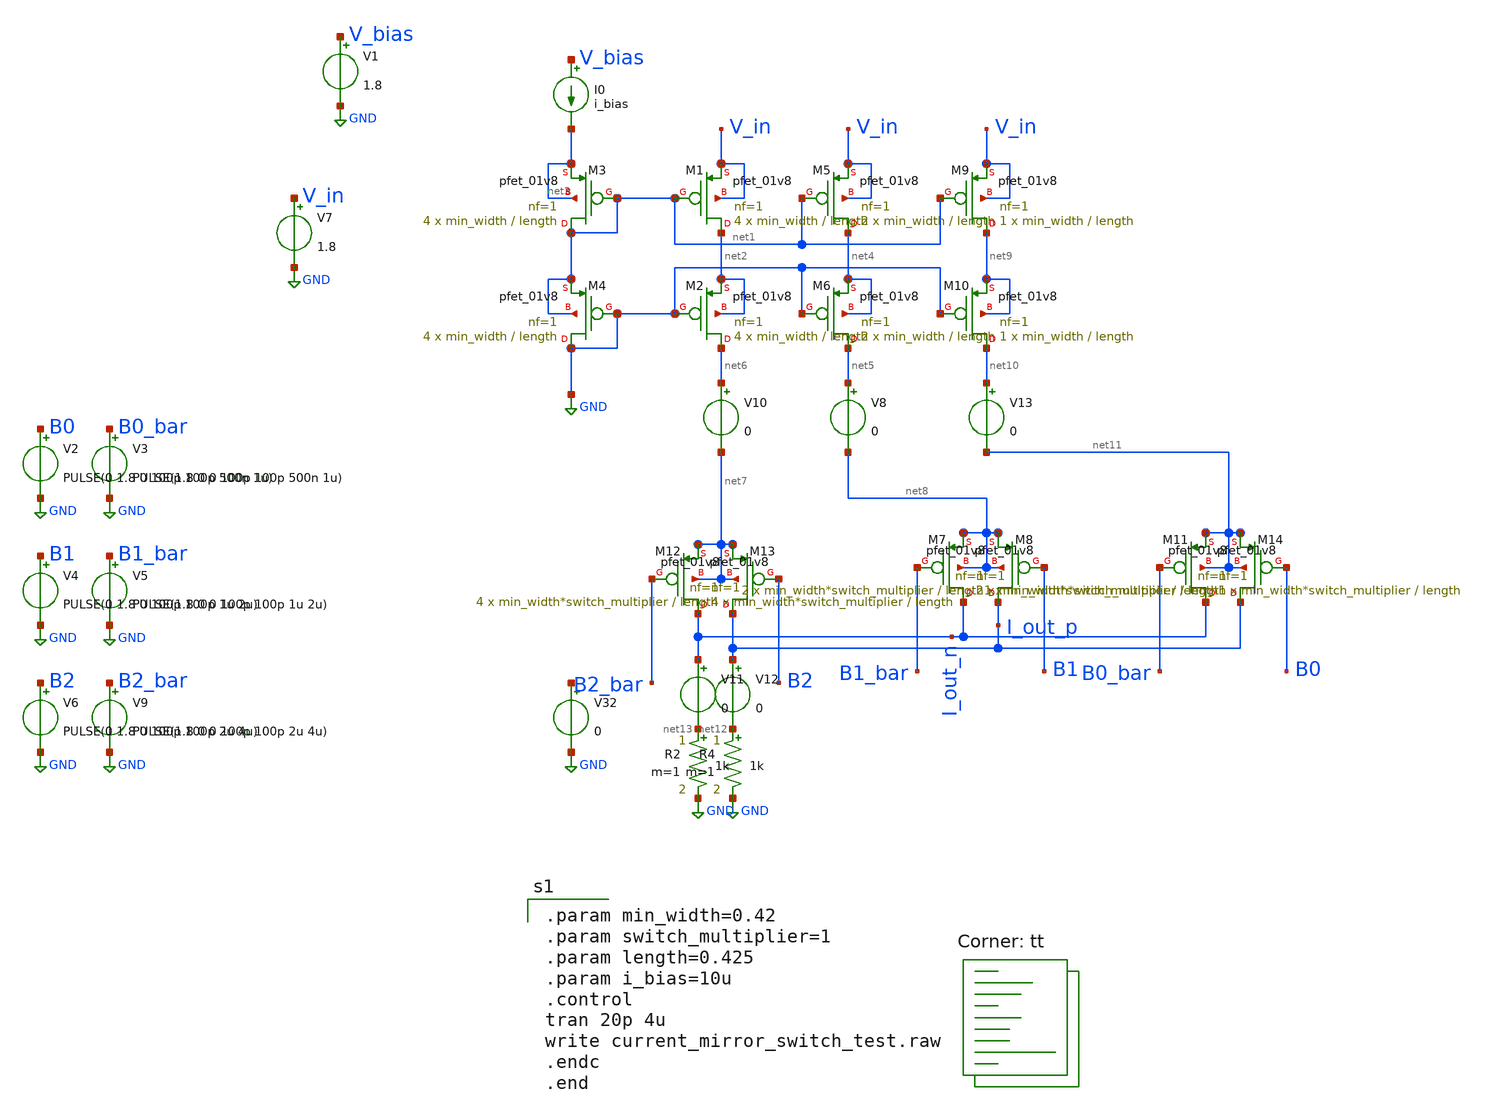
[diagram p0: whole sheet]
** sch_path: analog/schematics/testbenches/current_mirror_switch_test.sch
**.subckt current_mirror_switch_test
XM1 net2 net1 V_in V_in sky130_fd_pr__pfet_01v8 L=length W=min_width nf=1 ad='int((nf+1)/2) * W/nf * 0.29'
+ as='int((nf+2)/2) * W/nf * 0.29' pd='2*int((nf+1)/2) * (W/nf + 0.29)' ps='2*int((nf+2)/2) * (W/nf + 0.29)'
+ nrd='0.29 / W' nrs='0.29 / W' sa=0 sb=0 sd=0 mult=4 m=4
XM2 net6 GND net2 net2 sky130_fd_pr__pfet_01v8 L=length W=min_width nf=1 ad='int((nf+1)/2) * W/nf * 0.29'
+ as='int((nf+2)/2) * W/nf * 0.29' pd='2*int((nf+1)/2) * (W/nf + 0.29)' ps='2*int((nf+2)/2) * (W/nf + 0.29)'
+ nrd='0.29 / W' nrs='0.29 / W' sa=0 sb=0 sd=0 mult=4 m=4
XM3 net1 net1 net3 net3 sky130_fd_pr__pfet_01v8 L=length W=min_width nf=1 ad='int((nf+1)/2) * W/nf * 0.29'
+ as='int((nf+2)/2) * W/nf * 0.29' pd='2*int((nf+1)/2) * (W/nf + 0.29)' ps='2*int((nf+2)/2) * (W/nf + 0.29)'
+ nrd='0.29 / W' nrs='0.29 / W' sa=0 sb=0 sd=0 mult=4 m=4
XM4 GND GND net1 net1 sky130_fd_pr__pfet_01v8 L=length W=min_width nf=1 ad='int((nf+1)/2) * W/nf * 0.29'
+ as='int((nf+2)/2) * W/nf * 0.29' pd='2*int((nf+1)/2) * (W/nf + 0.29)' ps='2*int((nf+2)/2) * (W/nf + 0.29)'
+ nrd='0.29 / W' nrs='0.29 / W' sa=0 sb=0 sd=0 mult=4 m=4
XM5 net4 net1 V_in V_in sky130_fd_pr__pfet_01v8 L=length W=min_width nf=1 ad='int((nf+1)/2) * W/nf * 0.29'
+ as='int((nf+2)/2) * W/nf * 0.29' pd='2*int((nf+1)/2) * (W/nf + 0.29)' ps='2*int((nf+2)/2) * (W/nf + 0.29)'
+ nrd='0.29 / W' nrs='0.29 / W' sa=0 sb=0 sd=0 mult=2 m=2
XM6 net5 GND net4 net4 sky130_fd_pr__pfet_01v8 L=length W=min_width nf=1 ad='int((nf+1)/2) * W/nf * 0.29'
+ as='int((nf+2)/2) * W/nf * 0.29' pd='2*int((nf+1)/2) * (W/nf + 0.29)' ps='2*int((nf+2)/2) * (W/nf + 0.29)'
+ nrd='0.29 / W' nrs='0.29 / W' sa=0 sb=0 sd=0 mult=2 m=2
V2 B0 GND PULSE(0 1.8 0 100p 100p 500n 1u)
V3 B0_bar GND PULSE(1.8 0 0 100p 100p 500n 1u)
V4 B1 GND PULSE(0 1.8 0 100p 100p 1u 2u)
V5 B1_bar GND PULSE(1.8 0 0 100p 100p 1u 2u)
V7 V_in GND 1.8
V8 net5 net8 0
XM12 I_out_n B2_bar net7 net7 sky130_fd_pr__pfet_01v8 L=length W=min_width*switch_multiplier nf=1 ad='int((nf+1)/2) * W/nf * 0.29'
+ as='int((nf+2)/2) * W/nf * 0.29' pd='2*int((nf+1)/2) * (W/nf + 0.29)' ps='2*int((nf+2)/2) * (W/nf + 0.29)'
+ nrd='0.29 / W' nrs='0.29 / W' sa=0 sb=0 sd=0 mult=4 m=4
XM13 I_out_p B2 net7 net7 sky130_fd_pr__pfet_01v8 L=length W=min_width*switch_multiplier nf=1 ad='int((nf+1)/2) * W/nf * 0.29'
+ as='int((nf+2)/2) * W/nf * 0.29' pd='2*int((nf+1)/2) * (W/nf + 0.29)' ps='2*int((nf+2)/2) * (W/nf + 0.29)'
+ nrd='0.29 / W' nrs='0.29 / W' sa=0 sb=0 sd=0 mult=4 m=4
R4 net12 GND 1k m=1
V10 net6 net7 0
V11 I_out_n net13 0
V12 I_out_p net12 0
XM7 I_out_n B1_bar net8 net8 sky130_fd_pr__pfet_01v8 L=length W=min_width*switch_multiplier nf=1 ad='int((nf+1)/2) * W/nf * 0.29'
+ as='int((nf+2)/2) * W/nf * 0.29' pd='2*int((nf+1)/2) * (W/nf + 0.29)' ps='2*int((nf+2)/2) * (W/nf + 0.29)'
+ nrd='0.29 / W' nrs='0.29 / W' sa=0 sb=0 sd=0 mult=2 m=2
XM8 I_out_p B1 net8 net8 sky130_fd_pr__pfet_01v8 L=length W=min_width*switch_multiplier nf=1 ad='int((nf+1)/2) * W/nf * 0.29'
+ as='int((nf+2)/2) * W/nf * 0.29' pd='2*int((nf+1)/2) * (W/nf + 0.29)' ps='2*int((nf+2)/2) * (W/nf + 0.29)'
+ nrd='0.29 / W' nrs='0.29 / W' sa=0 sb=0 sd=0 mult=2 m=2
V6 B2 GND PULSE(0 1.8 0 100p 100p 2u 4u)
V9 B2_bar GND PULSE(1.8 0 0 100p 100p 2u 4u)
XM9 net9 net1 V_in V_in sky130_fd_pr__pfet_01v8 L=length W=min_width nf=1 ad='int((nf+1)/2) * W/nf * 0.29'
+ as='int((nf+2)/2) * W/nf * 0.29' pd='2*int((nf+1)/2) * (W/nf + 0.29)' ps='2*int((nf+2)/2) * (W/nf + 0.29)'
+ nrd='0.29 / W' nrs='0.29 / W' sa=0 sb=0 sd=0 mult=1 m=1
XM10 net10 GND net9 net9 sky130_fd_pr__pfet_01v8 L=length W=min_width nf=1 ad='int((nf+1)/2) * W/nf * 0.29'
+ as='int((nf+2)/2) * W/nf * 0.29' pd='2*int((nf+1)/2) * (W/nf + 0.29)' ps='2*int((nf+2)/2) * (W/nf + 0.29)'
+ nrd='0.29 / W' nrs='0.29 / W' sa=0 sb=0 sd=0 mult=1 m=1
V13 net10 net11 0
XM11 I_out_n B0_bar net11 net11 sky130_fd_pr__pfet_01v8 L=length W=min_width*switch_multiplier nf=1 ad='int((nf+1)/2) * W/nf * 0.29'
+ as='int((nf+2)/2) * W/nf * 0.29' pd='2*int((nf+1)/2) * (W/nf + 0.29)' ps='2*int((nf+2)/2) * (W/nf + 0.29)'
+ nrd='0.29 / W' nrs='0.29 / W' sa=0 sb=0 sd=0 mult=1 m=1
XM14 I_out_p B0 net11 net11 sky130_fd_pr__pfet_01v8 L=length W=min_width*switch_multiplier nf=1 ad='int((nf+1)/2) * W/nf * 0.29'
+ as='int((nf+2)/2) * W/nf * 0.29' pd='2*int((nf+1)/2) * (W/nf + 0.29)' ps='2*int((nf+2)/2) * (W/nf + 0.29)'
+ nrd='0.29 / W' nrs='0.29 / W' sa=0 sb=0 sd=0 mult=1 m=1
R2 net13 GND 1k m=1
I0 V_bias net3 i_bias
V1 V_bias GND 1.8
V32 net14 GND 0
**** begin user architecture code

.param min_width=0.42
.param switch_multiplier=1
.param length=0.425
.param i_bias=10u
.control
tran 20p 4u
write current_mirror_switch_test.raw
.endc
.end

.lib $::SKYWATER_MODELS/sky130.lib.spice tt
**** end user architecture code
**.ends
.GLOBAL GND
.end
